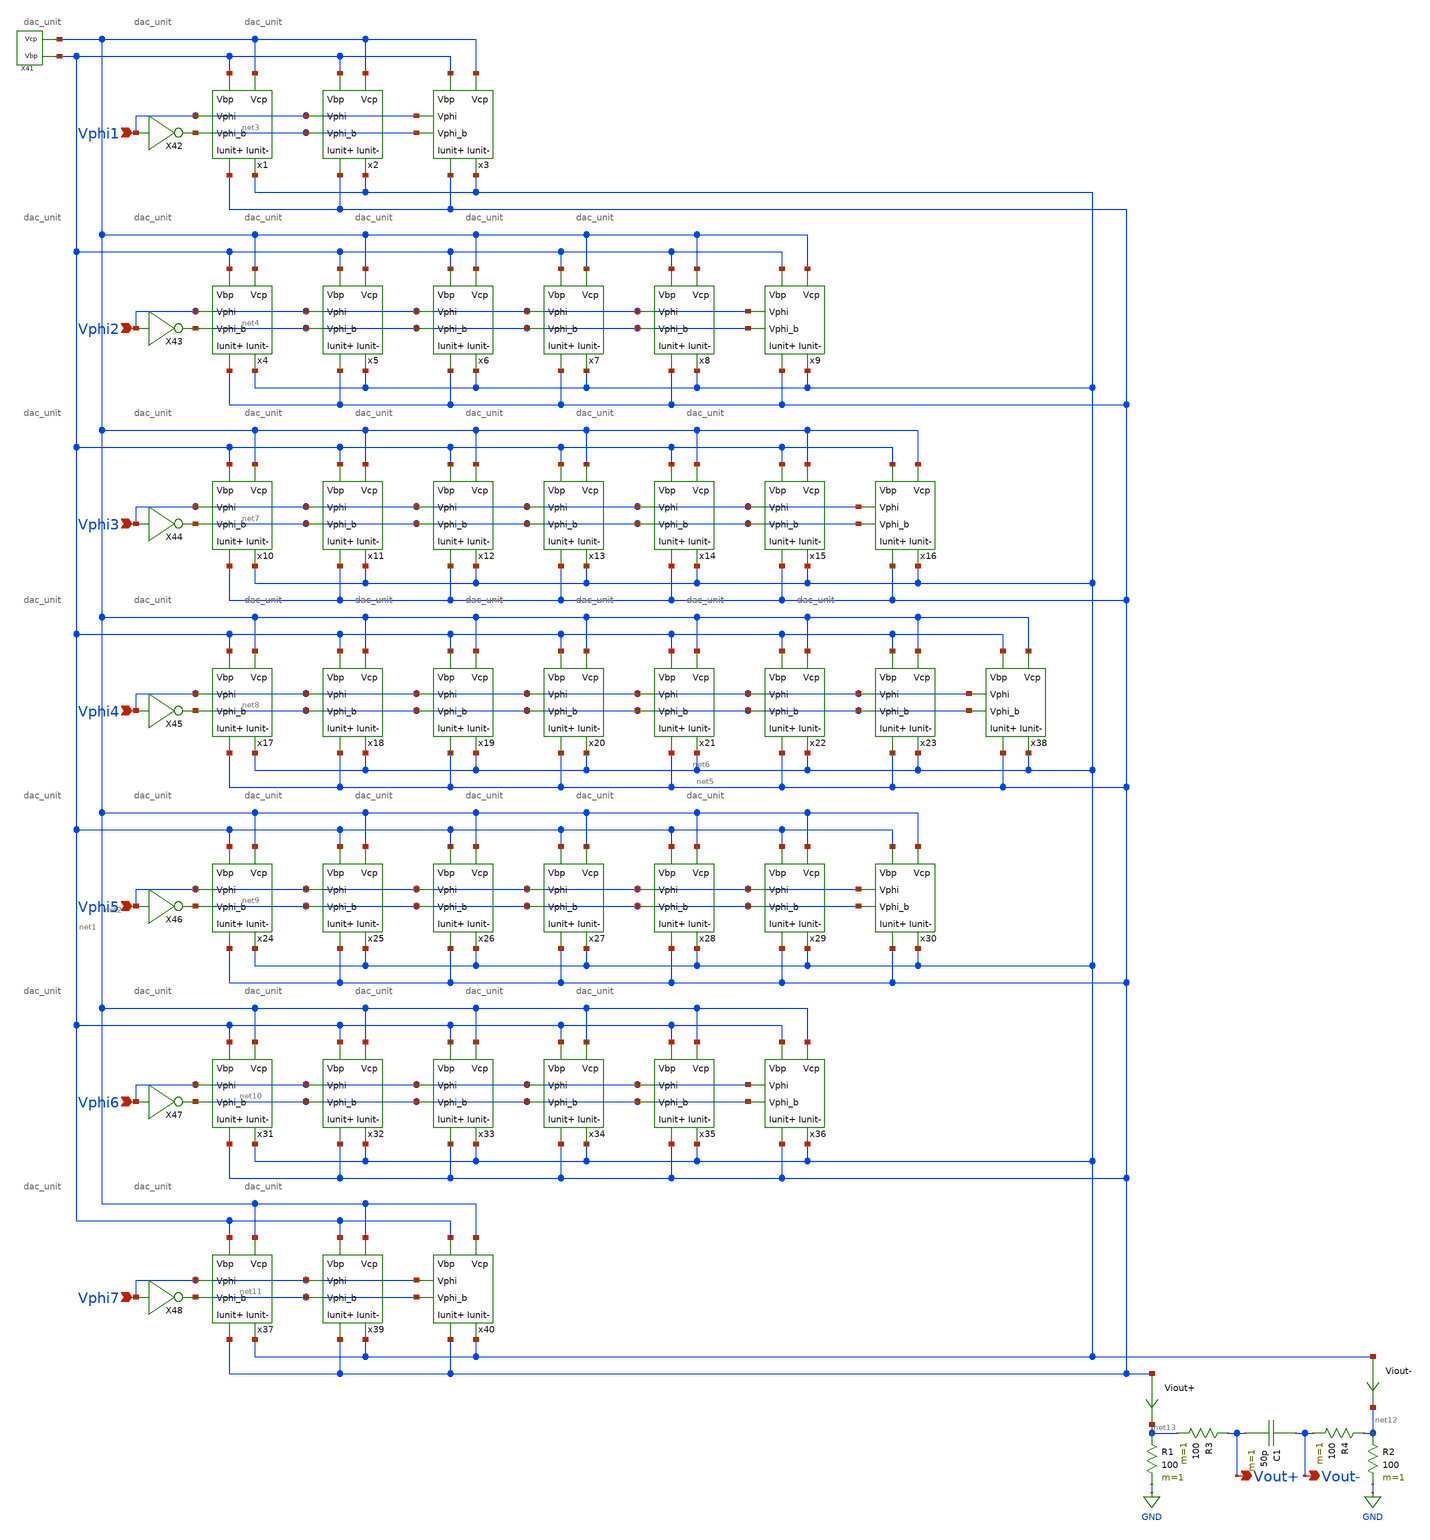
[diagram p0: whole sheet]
** sch_path: simulation/dac.sch
**.subckt dac Vphi1 Vphi2 Vphi3 Vphi4 Vphi5 Vphi6 Vphi7 Vout+ Vout-
*.ipin Vphi1
*.ipin Vphi2
*.ipin Vphi3
*.ipin Vphi4
*.ipin Vphi5
*.ipin Vphi6
*.ipin Vphi7
*.opin Vout+
*.opin Vout-
x1 net1 net2 net5 net6 Vphi1 net3 dac_unit
x2 net1 net2 net5 net6 Vphi1 net3 dac_unit
x3 net1 net2 net5 net6 Vphi1 net3 dac_unit
x4 net1 net2 net5 net6 Vphi2 net4 dac_unit
x5 net1 net2 net5 net6 Vphi2 net4 dac_unit
x6 net1 net2 net5 net6 Vphi2 net4 dac_unit
x7 net1 net2 net5 net6 Vphi2 net4 dac_unit
x8 net1 net2 net5 net6 Vphi2 net4 dac_unit
x9 net1 net2 net5 net6 Vphi2 net4 dac_unit
x10 net1 net2 net5 net6 Vphi3 net7 dac_unit
x11 net1 net2 net5 net6 Vphi3 net7 dac_unit
x12 net1 net2 net5 net6 Vphi3 net7 dac_unit
x13 net1 net2 net5 net6 Vphi3 net7 dac_unit
x14 net1 net2 net5 net6 Vphi3 net7 dac_unit
x15 net1 net2 net5 net6 Vphi3 net7 dac_unit
x16 net1 net2 net5 net6 Vphi3 net7 dac_unit
x17 net1 net2 net5 net6 Vphi4 net8 dac_unit
x18 net1 net2 net5 net6 Vphi4 net8 dac_unit
x19 net1 net2 net5 net6 Vphi4 net8 dac_unit
x20 net1 net2 net5 net6 Vphi4 net8 dac_unit
x21 net1 net2 net5 net6 Vphi4 net8 dac_unit
x22 net1 net2 net5 net6 Vphi4 net8 dac_unit
x23 net1 net2 net5 net6 Vphi4 net8 dac_unit
x24 net1 net2 net5 net6 Vphi5 net9 dac_unit
x25 net1 net2 net5 net6 Vphi5 net9 dac_unit
x26 net1 net2 net5 net6 Vphi5 net9 dac_unit
x27 net1 net2 net5 net6 Vphi5 net9 dac_unit
x28 net1 net2 net5 net6 Vphi5 net9 dac_unit
x29 net1 net2 net5 net6 Vphi5 net9 dac_unit
x30 net1 net2 net5 net6 Vphi5 net9 dac_unit
x31 net1 net2 net5 net6 Vphi6 net10 dac_unit
x32 net1 net2 net5 net6 Vphi6 net10 dac_unit
x33 net1 net2 net5 net6 Vphi6 net10 dac_unit
x34 net1 net2 net5 net6 Vphi6 net10 dac_unit
x35 net1 net2 net5 net6 Vphi6 net10 dac_unit
x36 net1 net2 net5 net6 Vphi6 net10 dac_unit
x38 net1 net2 net5 net6 Vphi4 net8 dac_unit
x37 net1 net2 net5 net6 Vphi7 net11 dac_unit
x39 net1 net2 net5 net6 Vphi7 net11 dac_unit
x40 net1 net2 net5 net6 Vphi7 net11 dac_unit
X41 net2 net1 v_gen_lds
X42 Vphi1 net3 inverter
R1 net13 GND 100 m=1
R2 net12 GND 100 m=1
R3 Vout+ net13 100 m=1
R4 net12 Vout- 100 m=1
C1 Vout- Vout+ 50p m=1
Viout+ net5 net13 0
.save i(viout+)
Viout- net6 net12 0
.save i(viout-)
X43 Vphi2 net4 inverter
X44 Vphi3 net7 inverter
X45 Vphi4 net8 inverter
X46 Vphi5 net9 inverter
X47 Vphi6 net10 inverter
X48 Vphi7 net11 inverter
**.ends

* expanding   symbol:  ./dac/dac_unit.sym # of pins=6
** sym_path: simulation/dac/dac_unit.sym
** sch_path: simulation/dac/dac_unit.sch
.subckt dac_unit Vbp Vcp Iunit+ Iunit- Vphi Vphi_b
*.ipin Vphi
*.ipin Vbp
*.ipin Vcp
*.opin Iunit-
*.opin Iunit+
*.ipin Vphi_b
XM1 net1 Vbp VDD VDD sky130_fd_pr__pfet_01v8 L=0.5 W=12 nf=1 ad='int((nf+1)/2) * W/nf * 0.29' as='int((nf+2)/2) * W/nf * 0.29'
+ pd='2*int((nf+1)/2) * (W/nf + 0.29)' ps='2*int((nf+2)/2) * (W/nf + 0.29)' nrd='0.29 / W' nrs='0.29 / W'
+ sa=0 sb=0 sd=0 mult=1 m=1
XM2 net2 Vcp net1 VDD sky130_fd_pr__pfet_01v8 L=0.5 W=12 nf=1 ad='int((nf+1)/2) * W/nf * 0.29' as='int((nf+2)/2) * W/nf * 0.29'
+ pd='2*int((nf+1)/2) * (W/nf + 0.29)' ps='2*int((nf+2)/2) * (W/nf + 0.29)' nrd='0.29 / W' nrs='0.29 / W'
+ sa=0 sb=0 sd=0 mult=1 m=1
XM3 Iunit- Vphi net2 VDD sky130_fd_pr__pfet_01v8 L=0.5 W=12 nf=1 ad='int((nf+1)/2) * W/nf * 0.29' as='int((nf+2)/2) * W/nf * 0.29'
+ pd='2*int((nf+1)/2) * (W/nf + 0.29)' ps='2*int((nf+2)/2) * (W/nf + 0.29)' nrd='0.29 / W' nrs='0.29 / W'
+ sa=0 sb=0 sd=0 mult=1 m=1
XM4 Iunit+ Vphi_b net2 VDD sky130_fd_pr__pfet_01v8 L=0.5 W=12 nf=1 ad='int((nf+1)/2) * W/nf * 0.29' as='int((nf+2)/2) * W/nf * 0.29'
+ pd='2*int((nf+1)/2) * (W/nf + 0.29)' ps='2*int((nf+2)/2) * (W/nf + 0.29)' nrd='0.29 / W' nrs='0.29 / W'
+ sa=0 sb=0 sd=0 mult=1 m=1
.ends


* expanding   symbol:  ./dac/v_gen_lds.sym # of pins=2
** sym_path: simulation/dac/v_gen_lds.sym
** sch_path: simulation/dac/v_gen_lds.sch
.subckt v_gen_lds Vcp Vbp
*.opin Vcp
*.opin Vbp
XM25 net1 Vcp Vcp VDD sky130_fd_pr__pfet_01v8 L=0.5 W=12 nf=1 ad='int((nf+1)/2) * W/nf * 0.29' as='int((nf+2)/2) * W/nf * 0.29'
+ pd='2*int((nf+1)/2) * (W/nf + 0.29)' ps='2*int((nf+2)/2) * (W/nf + 0.29)' nrd='0.29 / W' nrs='0.29 / W'
+ sa=0 sb=0 sd=0 mult=1 m=1
XM26 Vcp net3 GND GND sky130_fd_pr__nfet_01v8 L=0.5 W=12 nf=1 ad='int((nf+1)/2) * W/nf * 0.29' as='int((nf+2)/2) * W/nf * 0.29'
+ pd='2*int((nf+1)/2) * (W/nf + 0.29)' ps='2*int((nf+2)/2) * (W/nf + 0.29)' nrd='0.29 / W' nrs='0.29 / W'
+ sa=0 sb=0 sd=0 mult=1 m=1
XM27 net2 net2 net1 VDD sky130_fd_pr__pfet_01v8 L=0.5 W=12 nf=1 ad='int((nf+1)/2) * W/nf * 0.29' as='int((nf+2)/2) * W/nf * 0.29'
+ pd='2*int((nf+1)/2) * (W/nf + 0.29)' ps='2*int((nf+2)/2) * (W/nf + 0.29)' nrd='0.29 / W' nrs='0.29 / W'
+ sa=0 sb=0 sd=0 mult=1 m=1
XM28 GND net3 net4 GND sky130_fd_pr__nfet_01v8 L=0.5 W=12 nf=1 ad='int((nf+1)/2) * W/nf * 0.29' as='int((nf+2)/2) * W/nf * 0.29'
+ pd='2*int((nf+1)/2) * (W/nf + 0.29)' ps='2*int((nf+2)/2) * (W/nf + 0.29)' nrd='0.29 / W' nrs='0.29 / W'
+ sa=0 sb=0 sd=0 mult=1 m=1
XM41 net1 net2 net2 VDD sky130_fd_pr__pfet_01v8 L=0.5 W=12 nf=1 ad='int((nf+1)/2) * W/nf * 0.29' as='int((nf+2)/2) * W/nf * 0.29'
+ pd='2*int((nf+1)/2) * (W/nf + 0.29)' ps='2*int((nf+2)/2) * (W/nf + 0.29)' nrd='0.29 / W' nrs='0.29 / W'
+ sa=0 sb=0 sd=0 mult=1 m=1
XM42 net4 net3 net5 GND sky130_fd_pr__nfet_01v8 L=0.5 W=12 nf=1 ad='int((nf+1)/2) * W/nf * 0.29' as='int((nf+2)/2) * W/nf * 0.29'
+ pd='2*int((nf+1)/2) * (W/nf + 0.29)' ps='2*int((nf+2)/2) * (W/nf + 0.29)' nrd='0.29 / W' nrs='0.29 / W'
+ sa=0 sb=0 sd=0 mult=1 m=1
XM43 net2 net2 net1 VDD sky130_fd_pr__pfet_01v8 L=0.5 W=12 nf=1 ad='int((nf+1)/2) * W/nf * 0.29' as='int((nf+2)/2) * W/nf * 0.29'
+ pd='2*int((nf+1)/2) * (W/nf + 0.29)' ps='2*int((nf+2)/2) * (W/nf + 0.29)' nrd='0.29 / W' nrs='0.29 / W'
+ sa=0 sb=0 sd=0 mult=1 m=1
XM44 net5 net3 net6 GND sky130_fd_pr__nfet_01v8 L=0.5 W=12 nf=1 ad='int((nf+1)/2) * W/nf * 0.29' as='int((nf+2)/2) * W/nf * 0.29'
+ pd='2*int((nf+1)/2) * (W/nf + 0.29)' ps='2*int((nf+2)/2) * (W/nf + 0.29)' nrd='0.29 / W' nrs='0.29 / W'
+ sa=0 sb=0 sd=0 mult=1 m=1
XM45 net1 net2 net2 VDD sky130_fd_pr__pfet_01v8 L=0.5 W=12 nf=1 ad='int((nf+1)/2) * W/nf * 0.29' as='int((nf+2)/2) * W/nf * 0.29'
+ pd='2*int((nf+1)/2) * (W/nf + 0.29)' ps='2*int((nf+2)/2) * (W/nf + 0.29)' nrd='0.29 / W' nrs='0.29 / W'
+ sa=0 sb=0 sd=0 mult=1 m=1
XM46 net6 net3 net7 GND sky130_fd_pr__nfet_01v8 L=0.5 W=12 nf=1 ad='int((nf+1)/2) * W/nf * 0.29' as='int((nf+2)/2) * W/nf * 0.29'
+ pd='2*int((nf+1)/2) * (W/nf + 0.29)' ps='2*int((nf+2)/2) * (W/nf + 0.29)' nrd='0.29 / W' nrs='0.29 / W'
+ sa=0 sb=0 sd=0 mult=1 m=1
XM47 VDD net2 net1 VDD sky130_fd_pr__pfet_01v8 L=0.5 W=12 nf=1 ad='int((nf+1)/2) * W/nf * 0.29' as='int((nf+2)/2) * W/nf * 0.29'
+ pd='2*int((nf+1)/2) * (W/nf + 0.29)' ps='2*int((nf+2)/2) * (W/nf + 0.29)' nrd='0.29 / W' nrs='0.29 / W'
+ sa=0 sb=0 sd=0 mult=1 m=1
XM48 net7 net3 net2 GND sky130_fd_pr__nfet_01v8 L=0.5 W=12 nf=1 ad='int((nf+1)/2) * W/nf * 0.29' as='int((nf+2)/2) * W/nf * 0.29'
+ pd='2*int((nf+1)/2) * (W/nf + 0.29)' ps='2*int((nf+2)/2) * (W/nf + 0.29)' nrd='0.29 / W' nrs='0.29 / W'
+ sa=0 sb=0 sd=0 mult=1 m=1
XM54 VDD Vbp Vbp VDD sky130_fd_pr__pfet_01v8 L=0.5 W=12 nf=1 ad='int((nf+1)/2) * W/nf * 0.29' as='int((nf+2)/2) * W/nf * 0.29'
+ pd='2*int((nf+1)/2) * (W/nf + 0.29)' ps='2*int((nf+2)/2) * (W/nf + 0.29)' nrd='0.29 / W' nrs='0.29 / W'
+ sa=0 sb=0 sd=0 mult=1 m=1
XM1 Vbp net3 GND GND sky130_fd_pr__nfet_01v8 L=0.5 W=12 nf=1 ad='int((nf+1)/2) * W/nf * 0.29' as='int((nf+2)/2) * W/nf * 0.29'
+ pd='2*int((nf+1)/2) * (W/nf + 0.29)' ps='2*int((nf+2)/2) * (W/nf + 0.29)' nrd='0.29 / W' nrs='0.29 / W'
+ sa=0 sb=0 sd=0 mult=1 m=1
XM2 net3 net3 GND GND sky130_fd_pr__nfet_01v8 L=0.5 W=12 nf=1 ad='int((nf+1)/2) * W/nf * 0.29' as='int((nf+2)/2) * W/nf * 0.29'
+ pd='2*int((nf+1)/2) * (W/nf + 0.29)' ps='2*int((nf+2)/2) * (W/nf + 0.29)' nrd='0.29 / W' nrs='0.29 / W'
+ sa=0 sb=0 sd=0 mult=1 m=1
XM3 Vcp VDD VDD VDD sky130_fd_pr__pfet_01v8 L=0.5 W=12 nf=1 ad='int((nf+1)/2) * W/nf * 0.29' as='int((nf+2)/2) * W/nf * 0.29'
+ pd='2*int((nf+1)/2) * (W/nf + 0.29)' ps='2*int((nf+2)/2) * (W/nf + 0.29)' nrd='0.29 / W' nrs='0.29 / W'
+ sa=0 sb=0 sd=0 mult=1 m=1
XM16 net8 net13 net13 VDD sky130_fd_pr__pfet_01v8 L=0.5 W=12 nf=1 ad='int((nf+1)/2) * W/nf * 0.29' as='int((nf+2)/2) * W/nf * 0.29'
+ pd='2*int((nf+1)/2) * (W/nf + 0.29)' ps='2*int((nf+2)/2) * (W/nf + 0.29)' nrd='0.29 / W' nrs='0.29 / W'
+ sa=0 sb=0 sd=0 mult=1 m=1
XM17 net13 net3 GND GND sky130_fd_pr__nfet_01v8 L=0.5 W=12 nf=1 ad='int((nf+1)/2) * W/nf * 0.29' as='int((nf+2)/2) * W/nf * 0.29'
+ pd='2*int((nf+1)/2) * (W/nf + 0.29)' ps='2*int((nf+2)/2) * (W/nf + 0.29)' nrd='0.29 / W' nrs='0.29 / W'
+ sa=0 sb=0 sd=0 mult=1 m=1
XM18 net2 net2 net8 VDD sky130_fd_pr__pfet_01v8 L=0.5 W=12 nf=1 ad='int((nf+1)/2) * W/nf * 0.29' as='int((nf+2)/2) * W/nf * 0.29'
+ pd='2*int((nf+1)/2) * (W/nf + 0.29)' ps='2*int((nf+2)/2) * (W/nf + 0.29)' nrd='0.29 / W' nrs='0.29 / W'
+ sa=0 sb=0 sd=0 mult=1 m=1
XM19 GND net3 net9 GND sky130_fd_pr__nfet_01v8 L=0.5 W=12 nf=1 ad='int((nf+1)/2) * W/nf * 0.29' as='int((nf+2)/2) * W/nf * 0.29'
+ pd='2*int((nf+1)/2) * (W/nf + 0.29)' ps='2*int((nf+2)/2) * (W/nf + 0.29)' nrd='0.29 / W' nrs='0.29 / W'
+ sa=0 sb=0 sd=0 mult=1 m=1
XM20 net8 net2 net2 VDD sky130_fd_pr__pfet_01v8 L=0.5 W=12 nf=1 ad='int((nf+1)/2) * W/nf * 0.29' as='int((nf+2)/2) * W/nf * 0.29'
+ pd='2*int((nf+1)/2) * (W/nf + 0.29)' ps='2*int((nf+2)/2) * (W/nf + 0.29)' nrd='0.29 / W' nrs='0.29 / W'
+ sa=0 sb=0 sd=0 mult=1 m=1
XM21 net9 net3 net10 GND sky130_fd_pr__nfet_01v8 L=0.5 W=12 nf=1 ad='int((nf+1)/2) * W/nf * 0.29' as='int((nf+2)/2) * W/nf * 0.29'
+ pd='2*int((nf+1)/2) * (W/nf + 0.29)' ps='2*int((nf+2)/2) * (W/nf + 0.29)' nrd='0.29 / W' nrs='0.29 / W'
+ sa=0 sb=0 sd=0 mult=1 m=1
XM22 net2 net2 net8 VDD sky130_fd_pr__pfet_01v8 L=0.5 W=12 nf=1 ad='int((nf+1)/2) * W/nf * 0.29' as='int((nf+2)/2) * W/nf * 0.29'
+ pd='2*int((nf+1)/2) * (W/nf + 0.29)' ps='2*int((nf+2)/2) * (W/nf + 0.29)' nrd='0.29 / W' nrs='0.29 / W'
+ sa=0 sb=0 sd=0 mult=1 m=1
XM23 net10 net3 net11 GND sky130_fd_pr__nfet_01v8 L=0.5 W=12 nf=1 ad='int((nf+1)/2) * W/nf * 0.29' as='int((nf+2)/2) * W/nf * 0.29'
+ pd='2*int((nf+1)/2) * (W/nf + 0.29)' ps='2*int((nf+2)/2) * (W/nf + 0.29)' nrd='0.29 / W' nrs='0.29 / W'
+ sa=0 sb=0 sd=0 mult=1 m=1
XM24 net8 net2 net2 VDD sky130_fd_pr__pfet_01v8 L=0.5 W=12 nf=1 ad='int((nf+1)/2) * W/nf * 0.29' as='int((nf+2)/2) * W/nf * 0.29'
+ pd='2*int((nf+1)/2) * (W/nf + 0.29)' ps='2*int((nf+2)/2) * (W/nf + 0.29)' nrd='0.29 / W' nrs='0.29 / W'
+ sa=0 sb=0 sd=0 mult=1 m=1
XM49 net11 net3 net12 GND sky130_fd_pr__nfet_01v8 L=0.5 W=12 nf=1 ad='int((nf+1)/2) * W/nf * 0.29' as='int((nf+2)/2) * W/nf * 0.29'
+ pd='2*int((nf+1)/2) * (W/nf + 0.29)' ps='2*int((nf+2)/2) * (W/nf + 0.29)' nrd='0.29 / W' nrs='0.29 / W'
+ sa=0 sb=0 sd=0 mult=1 m=1
XM50 VDD net2 net8 VDD sky130_fd_pr__pfet_01v8 L=0.5 W=12 nf=1 ad='int((nf+1)/2) * W/nf * 0.29' as='int((nf+2)/2) * W/nf * 0.29'
+ pd='2*int((nf+1)/2) * (W/nf + 0.29)' ps='2*int((nf+2)/2) * (W/nf + 0.29)' nrd='0.29 / W' nrs='0.29 / W'
+ sa=0 sb=0 sd=0 mult=1 m=1
XM51 net12 net3 net2 GND sky130_fd_pr__nfet_01v8 L=0.5 W=12 nf=1 ad='int((nf+1)/2) * W/nf * 0.29' as='int((nf+2)/2) * W/nf * 0.29'
+ pd='2*int((nf+1)/2) * (W/nf + 0.29)' ps='2*int((nf+2)/2) * (W/nf + 0.29)' nrd='0.29 / W' nrs='0.29 / W'
+ sa=0 sb=0 sd=0 mult=1 m=1
XM52 VDD Vbp Vbp VDD sky130_fd_pr__pfet_01v8 L=0.5 W=12 nf=1 ad='int((nf+1)/2) * W/nf * 0.29' as='int((nf+2)/2) * W/nf * 0.29'
+ pd='2*int((nf+1)/2) * (W/nf + 0.29)' ps='2*int((nf+2)/2) * (W/nf + 0.29)' nrd='0.29 / W' nrs='0.29 / W'
+ sa=0 sb=0 sd=0 mult=1 m=1
XM53 GND net3 Vbp GND sky130_fd_pr__nfet_01v8 L=0.5 W=12 nf=1 ad='int((nf+1)/2) * W/nf * 0.29' as='int((nf+2)/2) * W/nf * 0.29'
+ pd='2*int((nf+1)/2) * (W/nf + 0.29)' ps='2*int((nf+2)/2) * (W/nf + 0.29)' nrd='0.29 / W' nrs='0.29 / W'
+ sa=0 sb=0 sd=0 mult=1 m=1
XM55 net3 net3 GND GND sky130_fd_pr__nfet_01v8 L=0.5 W=12 nf=1 ad='int((nf+1)/2) * W/nf * 0.29' as='int((nf+2)/2) * W/nf * 0.29'
+ pd='2*int((nf+1)/2) * (W/nf + 0.29)' ps='2*int((nf+2)/2) * (W/nf + 0.29)' nrd='0.29 / W' nrs='0.29 / W'
+ sa=0 sb=0 sd=0 mult=1 m=1
XM56 net13 VDD VDD VDD sky130_fd_pr__pfet_01v8 L=0.5 W=12 nf=1 ad='int((nf+1)/2) * W/nf * 0.29' as='int((nf+2)/2) * W/nf * 0.29'
+ pd='2*int((nf+1)/2) * (W/nf + 0.29)' ps='2*int((nf+2)/2) * (W/nf + 0.29)' nrd='0.29 / W' nrs='0.29 / W'
+ sa=0 sb=0 sd=0 mult=1 m=1
Ib GND net3 2u
.ends


* expanding   symbol:  ./dac/inverter.sym # of pins=2
** sym_path: simulation/dac/inverter.sym
** sch_path: simulation/dac/inverter.sch
.subckt inverter A Y
*.ipin A
*.opin Y
XM1 Y A VDD VDD sky130_fd_pr__pfet_01v8 L=0.15 W=1 nf=1 ad='int((nf+1)/2) * W/nf * 0.29' as='int((nf+2)/2) * W/nf * 0.29'
+ pd='2*int((nf+1)/2) * (W/nf + 0.29)' ps='2*int((nf+2)/2) * (W/nf + 0.29)' nrd='0.29 / W' nrs='0.29 / W'
+ sa=0 sb=0 sd=0 mult=1 m=1
XM2 Y A GND GND sky130_fd_pr__nfet_01v8 L=0.15 W=1 nf=1 ad='int((nf+1)/2) * W/nf * 0.29' as='int((nf+2)/2) * W/nf * 0.29'
+ pd='2*int((nf+1)/2) * (W/nf + 0.29)' ps='2*int((nf+2)/2) * (W/nf + 0.29)' nrd='0.29 / W' nrs='0.29 / W'
+ sa=0 sb=0 sd=0 mult=1 m=1
.ends

.GLOBAL GND
.GLOBAL VDD
.end
